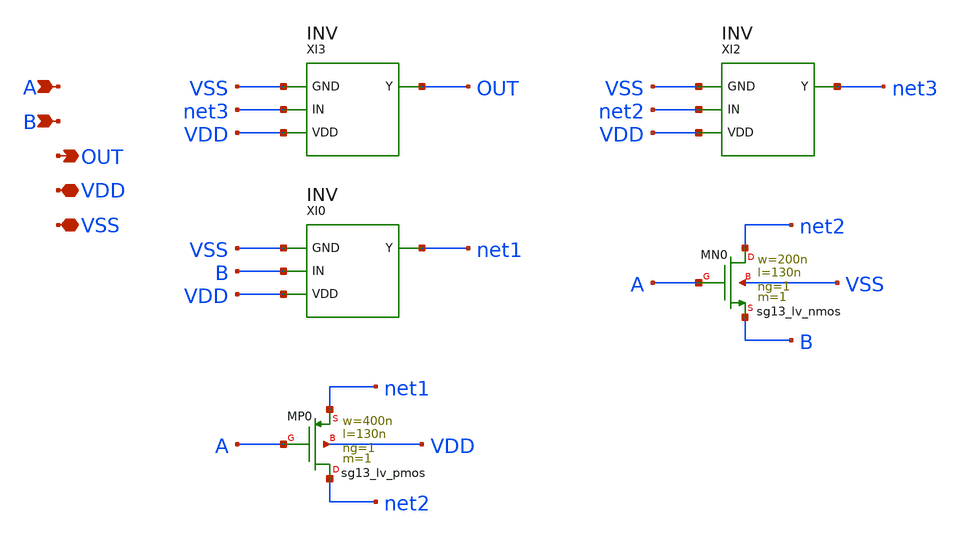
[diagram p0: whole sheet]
** sch_path: SoC6169-main/schematic/xschem/Xnor.sch
* Copyright 2026 USFQ CAM team
* Licensed under the Apache License, Version 2.0 (the "License");
* you may not use this file except in compliance with the License.
* You may obtain a copy of the License at
* https://www.apache.org/licenses/LICENSE-2.0
* Unless required by applicable law or agreed to in writing, software
* distributed under the License is distributed on an "AS IS" BASIS,
* WITHOUT WARRANTIES OR CONDITIONS OF ANY KIND, either express or implied.
* See the License for the specific language governing permissions and
* limitations under the License.
**.subckt Xnor A B OUT VDD VSS
*.ipin A
*.ipin B
*.opin OUT
*.iopin VDD
*.iopin VSS
XI3 VSS net3 VDD OUT INV
XI2 VSS net2 VDD net3 INV
XI0 VSS B VDD net1 INV
XMN0 net2 A B VSS sg13_lv_nmos w=200n l=130n ng=1 m=1 mm_ok=1
XMP0 net2 A net1 VDD sg13_lv_pmos w=400n l=130n ng=1 m=1 mm_ok=1
**.ends

* expanding   symbol:  INV.sym # of pins=4
** sym_path: SoC6169-main/schematic/xschem/INV.sym
** sch_path: SoC6169-main/schematic/xschem/INV.sch
.subckt INV GND IN VDD Y
*.iopin GND
*.ipin IN
*.iopin VDD
*.opin Y
XMN0 Y IN GND GND sg13_lv_nmos w=200n l=130n ng=1 m=1 mm_ok=1
XMP0 Y IN VDD VDD sg13_lv_pmos w=400n l=130n ng=1 m=1 mm_ok=1
.ends

.end
